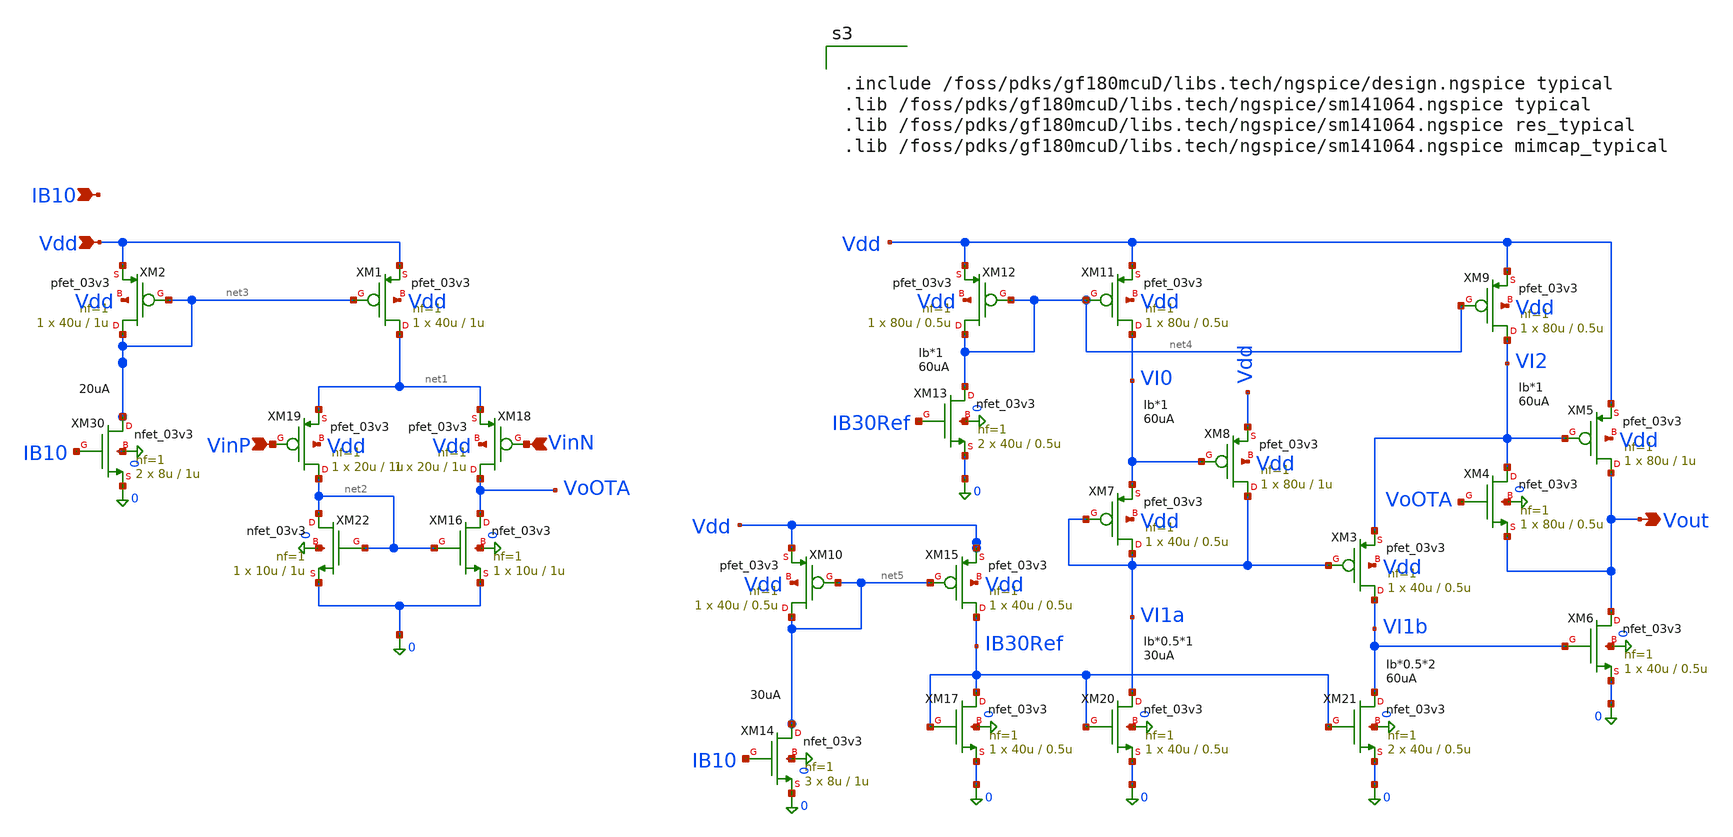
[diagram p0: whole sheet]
** sch_path: blocks/dac/cellv9/ota5_ab_buf_v1.sch
**.subckt ota5_ab_buf_v1 Vout VinP VinN Vdd IB10
*.opin Vout
*.ipin VinP
*.ipin VinN
*.ipin Vdd
*.ipin IB10
XM16 VoOTA net2 0 0 nfet_03v3 L=1u W=10u nf=1 ad='int((nf+1)/2) * W/nf * 0.18u' as='int((nf+2)/2) * W/nf * 0.18u'
+ pd='2*int((nf+1)/2) * (W/nf + 0.18u)' ps='2*int((nf+2)/2) * (W/nf + 0.18u)' nrd='0.18u / W' nrs='0.18u / W'
+ sa=0 sb=0 sd=0 m=1
XM18 VoOTA VinN net1 Vdd pfet_03v3 L=1u W=20u nf=1 ad='int((nf+1)/2) * W/nf * 0.18u' as='int((nf+2)/2) * W/nf * 0.18u'
+ pd='2*int((nf+1)/2) * (W/nf + 0.18u)' ps='2*int((nf+2)/2) * (W/nf + 0.18u)' nrd='0.18u / W' nrs='0.18u / W'
+ sa=0 sb=0 sd=0 m=1
XM19 net2 VinP net1 Vdd pfet_03v3 L=1u W=20u nf=1 ad='int((nf+1)/2) * W/nf * 0.18u' as='int((nf+2)/2) * W/nf * 0.18u'
+ pd='2*int((nf+1)/2) * (W/nf + 0.18u)' ps='2*int((nf+2)/2) * (W/nf + 0.18u)' nrd='0.18u / W' nrs='0.18u / W'
+ sa=0 sb=0 sd=0 m=1
XM22 net2 net2 0 0 nfet_03v3 L=1u W=10u nf=1 ad='int((nf+1)/2) * W/nf * 0.18u' as='int((nf+2)/2) * W/nf * 0.18u'
+ pd='2*int((nf+1)/2) * (W/nf + 0.18u)' ps='2*int((nf+2)/2) * (W/nf + 0.18u)' nrd='0.18u / W' nrs='0.18u / W'
+ sa=0 sb=0 sd=0 m=1
XM1 net1 net3 Vdd Vdd pfet_03v3 L=1u W=40u nf=1 ad='int((nf+1)/2) * W/nf * 0.18u' as='int((nf+2)/2) * W/nf * 0.18u'
+ pd='2*int((nf+1)/2) * (W/nf + 0.18u)' ps='2*int((nf+2)/2) * (W/nf + 0.18u)' nrd='0.18u / W' nrs='0.18u / W'
+ sa=0 sb=0 sd=0 m=1
XM2 net3 net3 Vdd Vdd pfet_03v3 L=1u W=40u nf=1 ad='int((nf+1)/2) * W/nf * 0.18u' as='int((nf+2)/2) * W/nf * 0.18u'
+ pd='2*int((nf+1)/2) * (W/nf + 0.18u)' ps='2*int((nf+2)/2) * (W/nf + 0.18u)' nrd='0.18u / W' nrs='0.18u / W'
+ sa=0 sb=0 sd=0 m=1
XM3 VI1b VI1a VI2 Vdd pfet_03v3 L=0.5u W=40u nf=1 ad='int((nf+1)/2) * W/nf * 0.18u' as='int((nf+2)/2) * W/nf * 0.18u'
+ pd='2*int((nf+1)/2) * (W/nf + 0.18u)' ps='2*int((nf+2)/2) * (W/nf + 0.18u)' nrd='0.18u / W' nrs='0.18u / W'
+ sa=0 sb=0 sd=0 m=1
XM4 VI2 VoOTA Vout 0 nfet_03v3 L=0.5u W=80u nf=1 ad='int((nf+1)/2) * W/nf * 0.18u' as='int((nf+2)/2) * W/nf * 0.18u'
+ pd='2*int((nf+1)/2) * (W/nf + 0.18u)' ps='2*int((nf+2)/2) * (W/nf + 0.18u)' nrd='0.18u / W' nrs='0.18u / W'
+ sa=0 sb=0 sd=0 m=1
XM5 Vout VI2 Vdd Vdd pfet_03v3 L=1u W=80u nf=1 ad='int((nf+1)/2) * W/nf * 0.18u' as='int((nf+2)/2) * W/nf * 0.18u'
+ pd='2*int((nf+1)/2) * (W/nf + 0.18u)' ps='2*int((nf+2)/2) * (W/nf + 0.18u)' nrd='0.18u / W' nrs='0.18u / W'
+ sa=0 sb=0 sd=0 m=1
XM6 Vout VI1b 0 0 nfet_03v3 L=0.5u W=40u nf=1 ad='int((nf+1)/2) * W/nf * 0.18u' as='int((nf+2)/2) * W/nf * 0.18u'
+ pd='2*int((nf+1)/2) * (W/nf + 0.18u)' ps='2*int((nf+2)/2) * (W/nf + 0.18u)' nrd='0.18u / W' nrs='0.18u / W'
+ sa=0 sb=0 sd=0 m=1
XM7 VI1a VI1a VI0 Vdd pfet_03v3 L=0.5u W=40u nf=1 ad='int((nf+1)/2) * W/nf * 0.18u' as='int((nf+2)/2) * W/nf * 0.18u'
+ pd='2*int((nf+1)/2) * (W/nf + 0.18u)' ps='2*int((nf+2)/2) * (W/nf + 0.18u)' nrd='0.18u / W' nrs='0.18u / W'
+ sa=0 sb=0 sd=0 m=1
XM8 VI1a VI0 Vdd Vdd pfet_03v3 L=1u W=80u nf=1 ad='int((nf+1)/2) * W/nf * 0.18u' as='int((nf+2)/2) * W/nf * 0.18u'
+ pd='2*int((nf+1)/2) * (W/nf + 0.18u)' ps='2*int((nf+2)/2) * (W/nf + 0.18u)' nrd='0.18u / W' nrs='0.18u / W'
+ sa=0 sb=0 sd=0 m=1
XM11 VI0 net4 Vdd Vdd pfet_03v3 L=0.5u W=80u nf=1 ad='int((nf+1)/2) * W/nf * 0.18u' as='int((nf+2)/2) * W/nf * 0.18u'
+ pd='2*int((nf+1)/2) * (W/nf + 0.18u)' ps='2*int((nf+2)/2) * (W/nf + 0.18u)' nrd='0.18u / W' nrs='0.18u / W'
+ sa=0 sb=0 sd=0 m=1
XM12 net4 net4 Vdd Vdd pfet_03v3 L=0.5u W=80u nf=1 ad='int((nf+1)/2) * W/nf * 0.18u' as='int((nf+2)/2) * W/nf * 0.18u'
+ pd='2*int((nf+1)/2) * (W/nf + 0.18u)' ps='2*int((nf+2)/2) * (W/nf + 0.18u)' nrd='0.18u / W' nrs='0.18u / W'
+ sa=0 sb=0 sd=0 m=1
XM9 VI2 net4 Vdd Vdd pfet_03v3 L=0.5u W=80u nf=1 ad='int((nf+1)/2) * W/nf * 0.18u' as='int((nf+2)/2) * W/nf * 0.18u'
+ pd='2*int((nf+1)/2) * (W/nf + 0.18u)' ps='2*int((nf+2)/2) * (W/nf + 0.18u)' nrd='0.18u / W' nrs='0.18u / W'
+ sa=0 sb=0 sd=0 m=1
XM10 net5 net5 Vdd Vdd pfet_03v3 L=0.5u W=40u nf=1 ad='int((nf+1)/2) * W/nf * 0.18u' as='int((nf+2)/2) * W/nf * 0.18u'
+ pd='2*int((nf+1)/2) * (W/nf + 0.18u)' ps='2*int((nf+2)/2) * (W/nf + 0.18u)' nrd='0.18u / W' nrs='0.18u / W'
+ sa=0 sb=0 sd=0 m=1
XM15 IB30Ref net5 Vdd Vdd pfet_03v3 L=0.5u W=40u nf=1 ad='int((nf+1)/2) * W/nf * 0.18u' as='int((nf+2)/2) * W/nf * 0.18u'
+ pd='2*int((nf+1)/2) * (W/nf + 0.18u)' ps='2*int((nf+2)/2) * (W/nf + 0.18u)' nrd='0.18u / W' nrs='0.18u / W'
+ sa=0 sb=0 sd=0 m=1
XM17 IB30Ref IB30Ref 0 0 nfet_03v3 L=0.5u W=40u nf=1 ad='int((nf+1)/2) * W/nf * 0.18u' as='int((nf+2)/2) * W/nf * 0.18u'
+ pd='2*int((nf+1)/2) * (W/nf + 0.18u)' ps='2*int((nf+2)/2) * (W/nf + 0.18u)' nrd='0.18u / W' nrs='0.18u / W'
+ sa=0 sb=0 sd=0 m=1
XM20 VI1a IB30Ref 0 0 nfet_03v3 L=0.5u W=40u nf=1 ad='int((nf+1)/2) * W/nf * 0.18u' as='int((nf+2)/2) * W/nf * 0.18u'
+ pd='2*int((nf+1)/2) * (W/nf + 0.18u)' ps='2*int((nf+2)/2) * (W/nf + 0.18u)' nrd='0.18u / W' nrs='0.18u / W'
+ sa=0 sb=0 sd=0 m=1
XM21 VI1b IB30Ref 0 0 nfet_03v3 L=0.5u W=40u nf=1 ad='int((nf+1)/2) * W/nf * 0.18u' as='int((nf+2)/2) * W/nf * 0.18u'
+ pd='2*int((nf+1)/2) * (W/nf + 0.18u)' ps='2*int((nf+2)/2) * (W/nf + 0.18u)' nrd='0.18u / W' nrs='0.18u / W'
+ sa=0 sb=0 sd=0 m=2
XM13 net4 IB30Ref 0 0 nfet_03v3 L=0.5u W=40u nf=1 ad='int((nf+1)/2) * W/nf * 0.18u' as='int((nf+2)/2) * W/nf * 0.18u'
+ pd='2*int((nf+1)/2) * (W/nf + 0.18u)' ps='2*int((nf+2)/2) * (W/nf + 0.18u)' nrd='0.18u / W' nrs='0.18u / W'
+ sa=0 sb=0 sd=0 m=2
XM30 net3 IB10 0 0 nfet_03v3 L=1u W=8u nf=1 ad='int((nf+1)/2) * W/nf * 0.18u' as='int((nf+2)/2) * W/nf * 0.18u'
+ pd='2*int((nf+1)/2) * (W/nf + 0.18u)' ps='2*int((nf+2)/2) * (W/nf + 0.18u)' nrd='0.18u / W' nrs='0.18u / W'
+ sa=0 sb=0 sd=0 m=2
XM14 net5 IB10 0 0 nfet_03v3 L=1u W=8u nf=1 ad='int((nf+1)/2) * W/nf * 0.18u' as='int((nf+2)/2) * W/nf * 0.18u'
+ pd='2*int((nf+1)/2) * (W/nf + 0.18u)' ps='2*int((nf+2)/2) * (W/nf + 0.18u)' nrd='0.18u / W' nrs='0.18u / W'
+ sa=0 sb=0 sd=0 m=3
**** begin user architecture code


.include /foss/pdks/gf180mcuD/libs.tech/ngspice/design.ngspice typical
.lib /foss/pdks/gf180mcuD/libs.tech/ngspice/sm141064.ngspice typical
.lib /foss/pdks/gf180mcuD/libs.tech/ngspice/sm141064.ngspice res_typical
.lib /foss/pdks/gf180mcuD/libs.tech/ngspice/sm141064.ngspice mimcap_typical


**** end user architecture code
**.ends
.end
